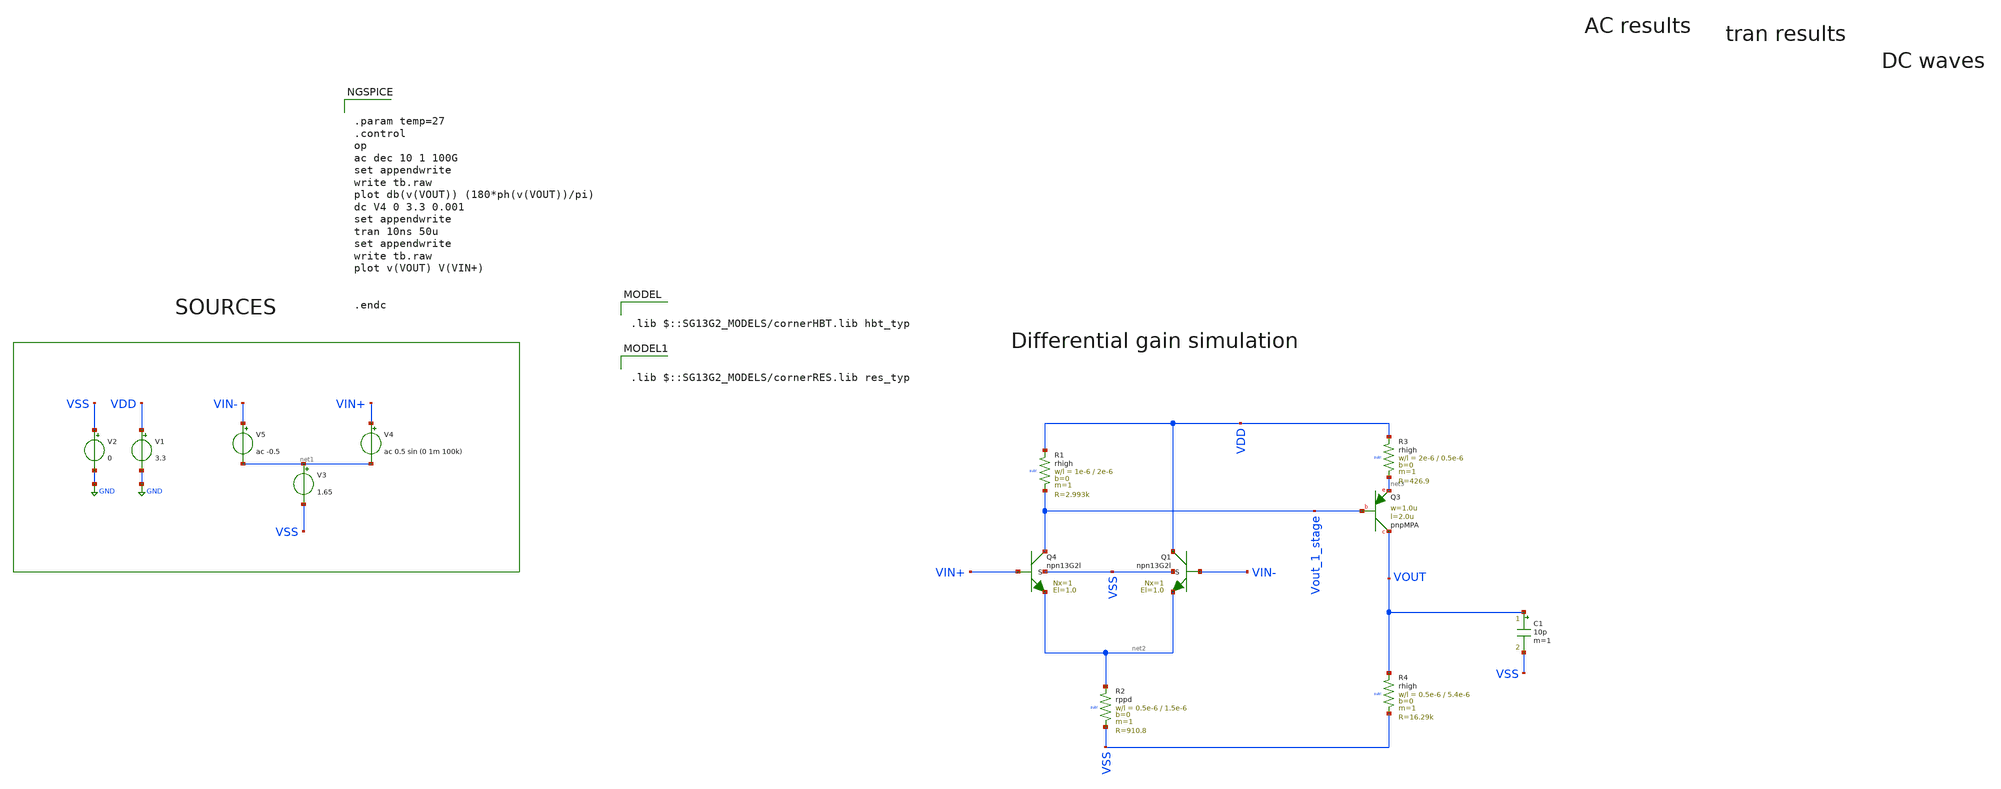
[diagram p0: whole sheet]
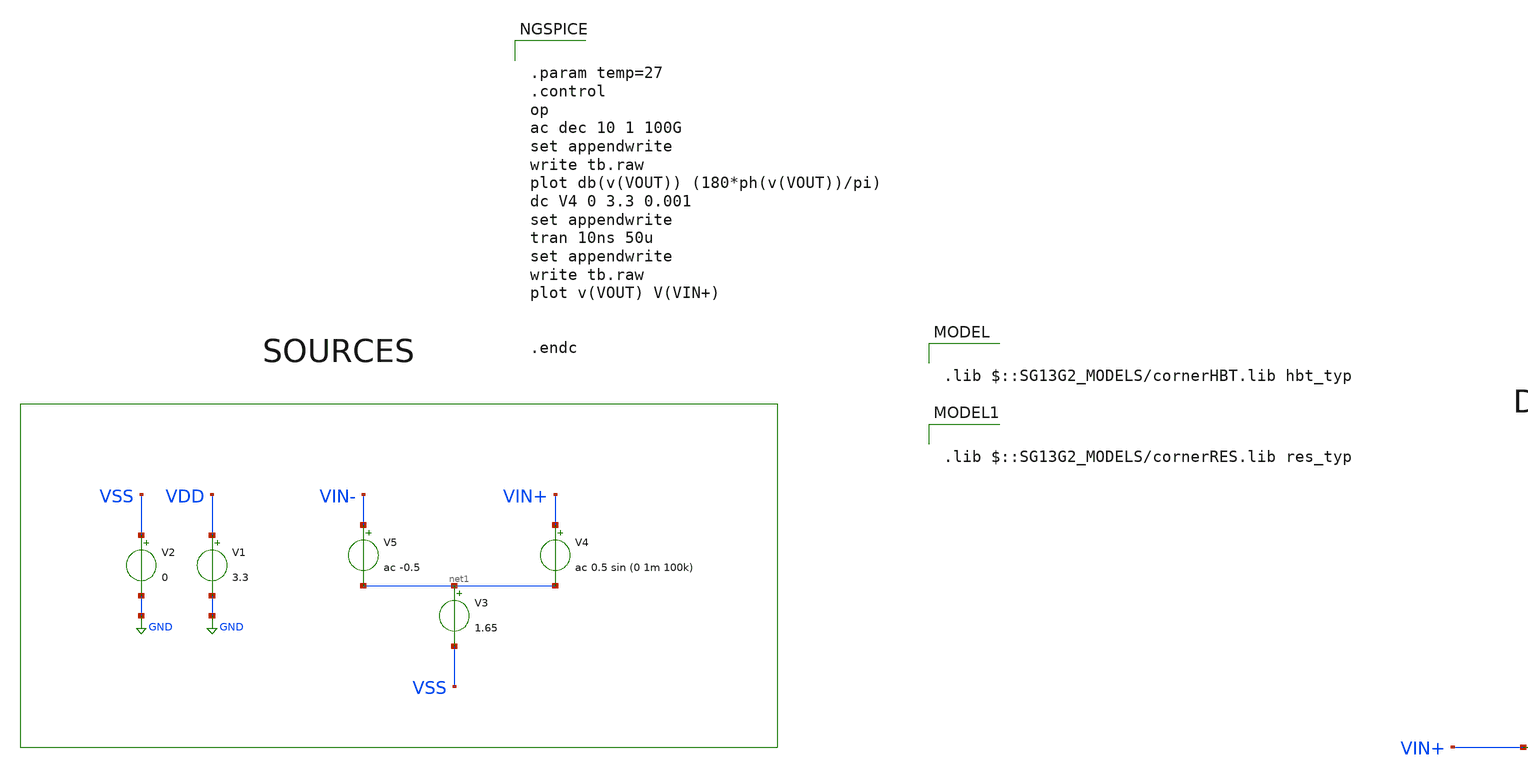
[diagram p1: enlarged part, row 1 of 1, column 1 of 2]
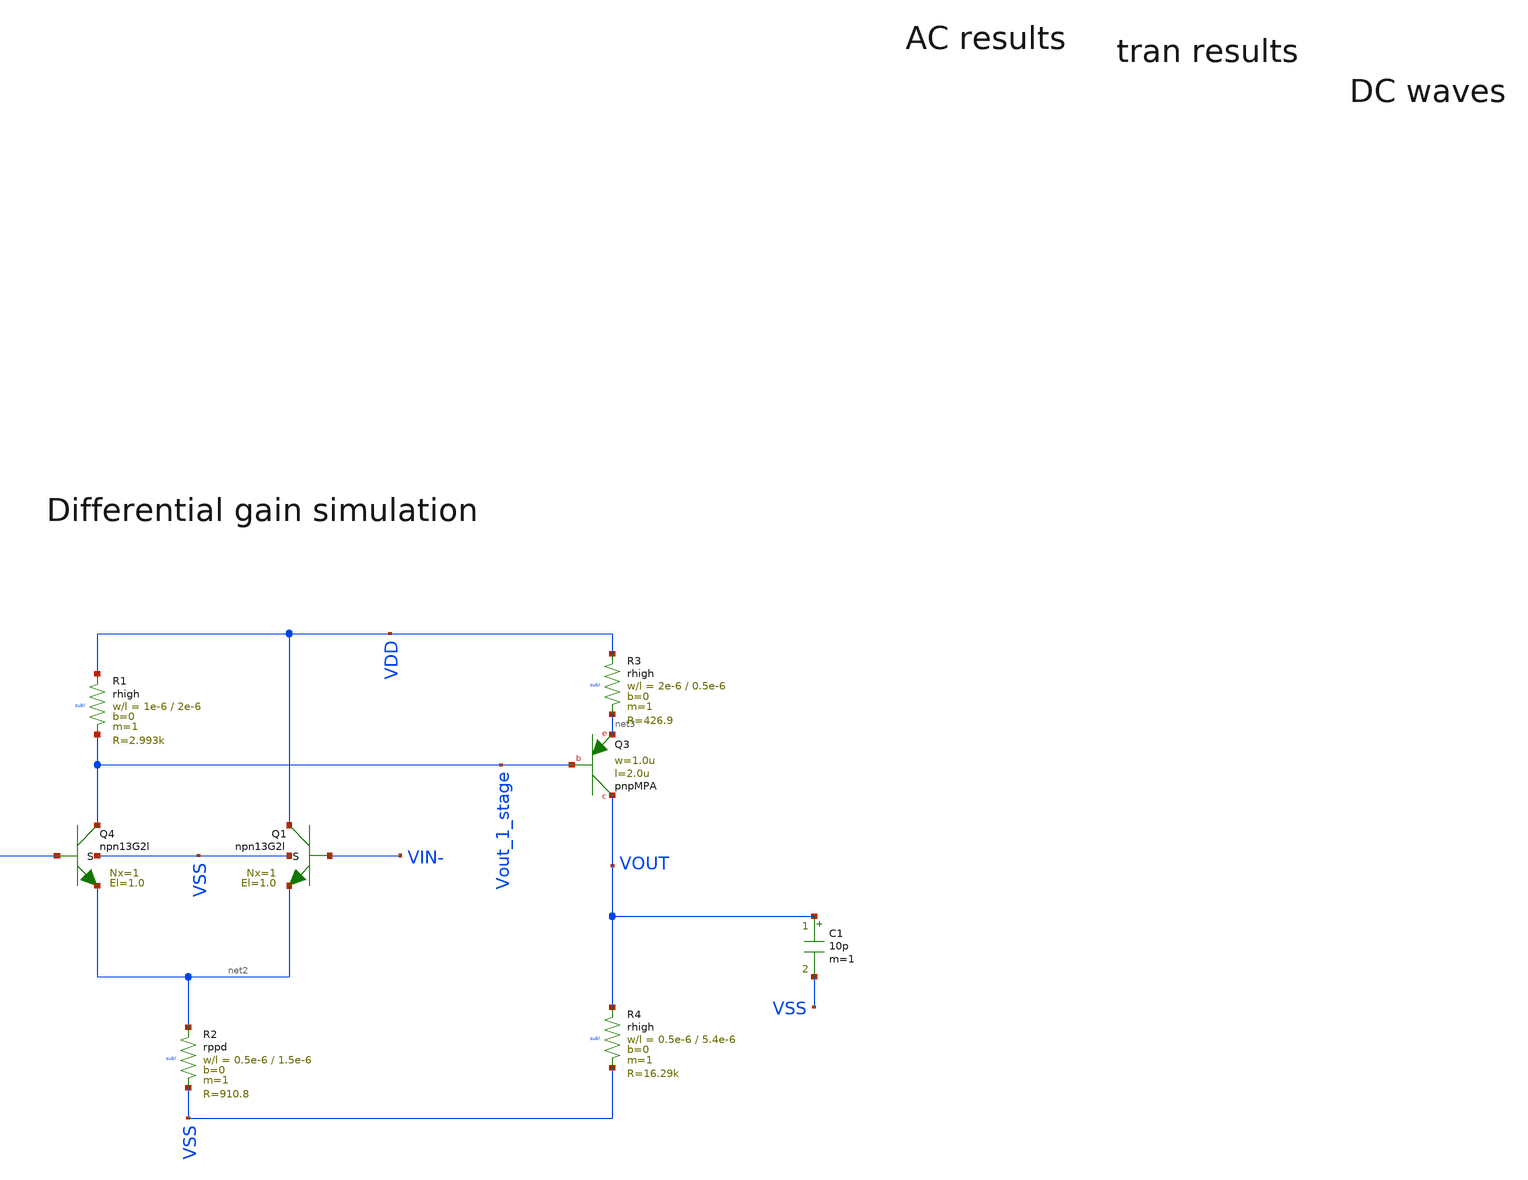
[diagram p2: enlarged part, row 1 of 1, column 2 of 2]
** sch_path: my_ip/testneches_ihp-sg13g2/single_ended_OTAS_testbenches/tb.sch
**.subckt tb
V1 VDD GND 3.3
V2 VSS GND 0
V3 net1 VSS 1.65
V4 VIN+ net1 ac 0.5 sin (0 1m 100k)
V5 VIN- net1 ac -0.5
C1 VOUT VSS 10p m=1
XR1 VDD Vout_1_stage sub! rhigh w=1e-6 l=2e-6 m=1 b=0 mm_ok=1
XR2 net2 VSS sub! rppd w=0.5e-6 l=1.5e-6 m=1 b=0 mm_ok=1
XQ3 VOUT Vout_1_stage net3 pnpMPA a=2p p=6u m=1
XR3 VDD net3 sub! rhigh w=2e-6 l=0.5e-6 m=1 b=0 mm_ok=1
XR4 VOUT VSS sub! rhigh w=0.5e-6 l=5.4e-6 m=1 b=0 mm_ok=1
XQ4 Vout_1_stage VIN+ net2 VSS npn13G2l Nx=1 El=1.0 mm_ok=1
XQ1 VDD VIN- net2 VSS npn13G2l Nx=1 El=1.0 mm_ok=1
**** begin user architecture code

.lib $::SG13G2_MODELS/cornerHBT.lib hbt_typ


.lib $::SG13G2_MODELS/cornerRES.lib res_typ



.param temp=27
.control
op
ac dec 10 1 100G
set appendwrite
write tb.raw
plot db(v(VOUT)) (180*ph(v(VOUT))/pi)
dc V4 0 3.3 0.001
set appendwrite
tran 10ns 50u
set appendwrite
write tb.raw
plot v(VOUT) V(VIN+)


.endc


**** end user architecture code
**.ends
.GLOBAL GND
.end
